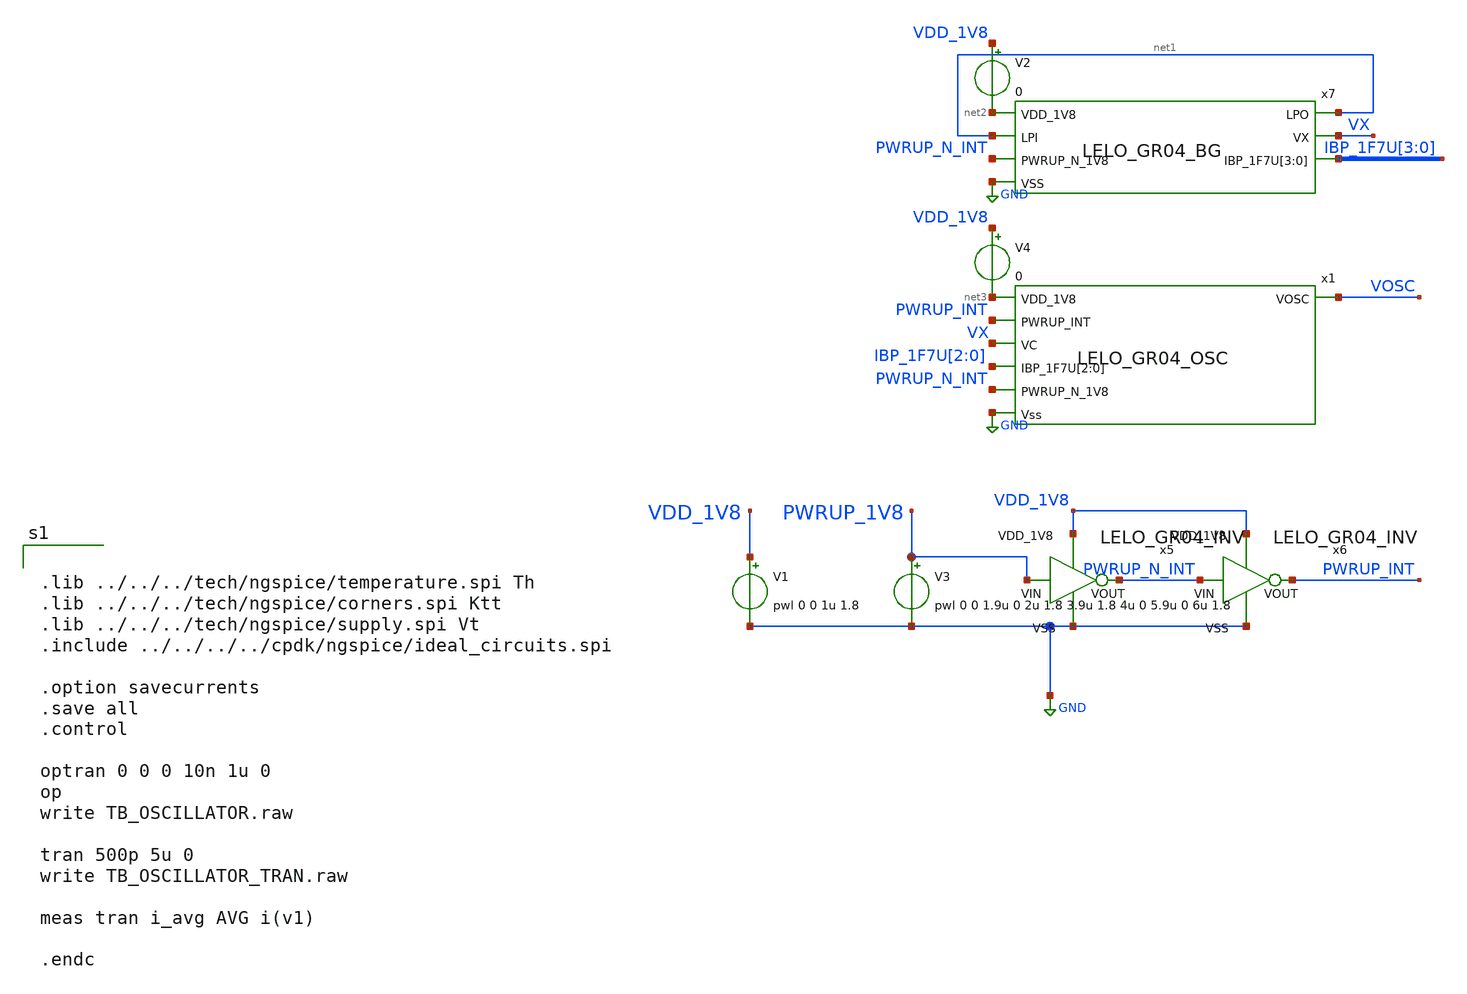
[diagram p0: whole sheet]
** sch_path: design/LELO_GR04_SKY130A/TB_OSCILLATOR.sch
**.subckt TB_OSCILLATOR
V1 VDD_1V8 GND pwl 0 0 1u 1.8
V3 PWRUP_1V8 GND pwl 0 0 1.9u 0 2u 1.8 3.9u 1.8 4u 0 5.9u 0 6u 1.8
x5 VDD_1V8 PWRUP_1V8 PWRUP_N_INT GND LELO_GR04_INV
x6 VDD_1V8 PWRUP_N_INT PWRUP_INT GND LELO_GR04_INV
x7 net2 net1 net1 VX PWRUP_N_INT IBP_1F7U[3] IBP_1F7U[2] IBP_1F7U[1] IBP_1F7U[0] GND LELO_GR04_BG
x1 VOSC net3 PWRUP_INT VX IBP_1F7U[2] IBP_1F7U[1] IBP_1F7U[0] PWRUP_N_INT GND LELO_GR04_OSC
V2 VDD_1V8 net2 0
V4 VDD_1V8 net3 0
**** begin user architecture code


.lib ../../../tech/ngspice/temperature.spi Th
.lib ../../../tech/ngspice/corners.spi Ktt
.lib ../../../tech/ngspice/supply.spi Vt
.include ../../../../cpdk/ngspice/ideal_circuits.spi

.option savecurrents
.save all
.control

optran 0 0 0 10n 1u 0
op
write TB_OSCILLATOR.raw

tran 500p 5u 0
write TB_OSCILLATOR_TRAN.raw

meas tran i_avg AVG i(v1)

.endc


**** end user architecture code
**.ends
.GLOBAL GND
.end
